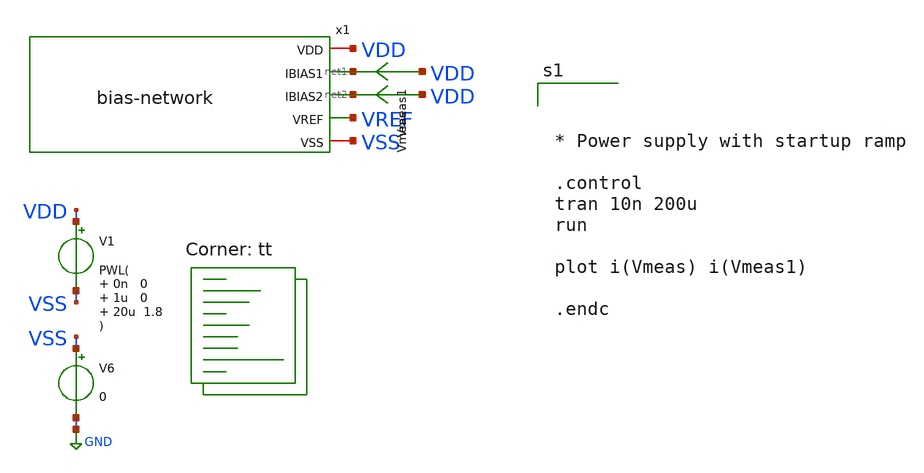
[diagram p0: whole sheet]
** sch_path: xschem/bias-net/testbench/tb_tran.sch
**.subckt tb_tran
V1 VDD VSS PWL( 0n 0 1u 0 20u 1.8
)
V6 VSS GND 0
x1 VDD net1 net2 VREF VSS bias-network
Vmeas VDD net2 0
.save i(vmeas)
Vmeas1 VDD net1 0
.save i(vmeas1)
**** begin user architecture code



* Power supply with startup ramp

.control
tran 10n 200u
run

plot i(Vmeas) i(Vmeas1)

.endc


.lib $::SKYWATER_MODELS/sky130.lib.spice tt
**** end user architecture code
**.ends

* expanding   symbol:
*+  /foss/designs/2026/tt_sky26b_ldo_andriansyah/xschem/bias-net/schematics/bias-network.sym # of pins=5
** sym_path: xschem/bias-net/schematics/bias-network.sym
** sch_path: xschem/bias-net/schematics/bias-network.sch
.subckt bias-network VDD IBIAS1 IBIAS2 VREF VSS
*.iopin VDD
*.iopin VSS
*.opin IBIAS1
*.opin IBIAS2
*.opin VREF
XM2 VREF VREF VSS VSS sky130_fd_pr__nfet_01v8 L=2 W=3 nf=4 ad='int((nf+1)/2) * W/nf * 0.29' as='int((nf+2)/2) * W/nf * 0.29'
+ pd='2*int((nf+1)/2) * (W/nf + 0.29)' ps='2*int((nf+2)/2) * (W/nf + 0.29)' nrd='0.29 / W' nrs='0.29 / W'
+ sa=0 sb=0 sd=0 mult=2 m=2
XR1 VREF net1 VSS sky130_fd_pr__res_xhigh_po_0p69 L=6.9 mult=1 m=1
XR2 net2 net1 VSS sky130_fd_pr__res_xhigh_po_0p69 L=6.9 mult=1 m=1
XR3 net2 net3 VSS sky130_fd_pr__res_xhigh_po_0p69 L=6.9 mult=1 m=1
XR4 net4 net3 VSS sky130_fd_pr__res_xhigh_po_0p69 L=6.9 mult=1 m=1
XR5 net4 net5 VSS sky130_fd_pr__res_xhigh_po_0p69 L=6.9 mult=1 m=1
XR6 net9 net10 VSS sky130_fd_pr__res_xhigh_po_0p69 L=6.9 mult=1 m=1
XR7 net9 net8 VSS sky130_fd_pr__res_xhigh_po_0p69 L=6.9 mult=1 m=1
XR8 net7 net8 VSS sky130_fd_pr__res_xhigh_po_0p69 L=6.9 mult=1 m=1
XR9 net7 net6 VSS sky130_fd_pr__res_xhigh_po_0p69 L=6.9 mult=1 m=1
XR10 net5 net6 VSS sky130_fd_pr__res_xhigh_po_0p69 L=6.9 mult=1 m=1
XM1 IBIAS1 VREF VSS VSS sky130_fd_pr__nfet_01v8 L=2 W=3 nf=4 ad='int((nf+1)/2) * W/nf * 0.29' as='int((nf+2)/2) * W/nf * 0.29'
+ pd='2*int((nf+1)/2) * (W/nf + 0.29)' ps='2*int((nf+2)/2) * (W/nf + 0.29)' nrd='0.29 / W' nrs='0.29 / W'
+ sa=0 sb=0 sd=0 mult=2 m=2
XM3 IBIAS2 VREF VSS VSS sky130_fd_pr__nfet_01v8 L=2 W=3 nf=4 ad='int((nf+1)/2) * W/nf * 0.29' as='int((nf+2)/2) * W/nf * 0.29'
+ pd='2*int((nf+1)/2) * (W/nf + 0.29)' ps='2*int((nf+2)/2) * (W/nf + 0.29)' nrd='0.29 / W' nrs='0.29 / W'
+ sa=0 sb=0 sd=0 mult=2 m=2
XR11 net10 net11 VSS sky130_fd_pr__res_xhigh_po_0p69 L=6.9 mult=1 m=1
XR12 net12 net11 VSS sky130_fd_pr__res_xhigh_po_0p69 L=6.9 mult=1 m=1
XR13 net12 net13 VSS sky130_fd_pr__res_xhigh_po_0p69 L=6.9 mult=1 m=1
XR14 net14 net13 VSS sky130_fd_pr__res_xhigh_po_0p69 L=6.9 mult=1 m=1
XR15 net14 net15 VSS sky130_fd_pr__res_xhigh_po_0p69 L=6.9 mult=1 m=1
XR16 net19 VDD VSS sky130_fd_pr__res_xhigh_po_0p69 L=6.9 mult=1 m=1
XR17 net19 net18 VSS sky130_fd_pr__res_xhigh_po_0p69 L=6.9 mult=1 m=1
XR18 net17 net18 VSS sky130_fd_pr__res_xhigh_po_0p69 L=6.9 mult=1 m=1
XR19 net17 net16 VSS sky130_fd_pr__res_xhigh_po_0p69 L=6.9 mult=1 m=1
XR20 net15 net16 VSS sky130_fd_pr__res_xhigh_po_0p69 L=6.9 mult=1 m=1
XR21 VSS VSS VSS sky130_fd_pr__res_xhigh_po_0p69 L=6.9 mult=1 m=1
XR22 VSS VSS VSS sky130_fd_pr__res_xhigh_po_0p69 L=6.9 mult=1 m=1
.ends

.GLOBAL GND
.end
